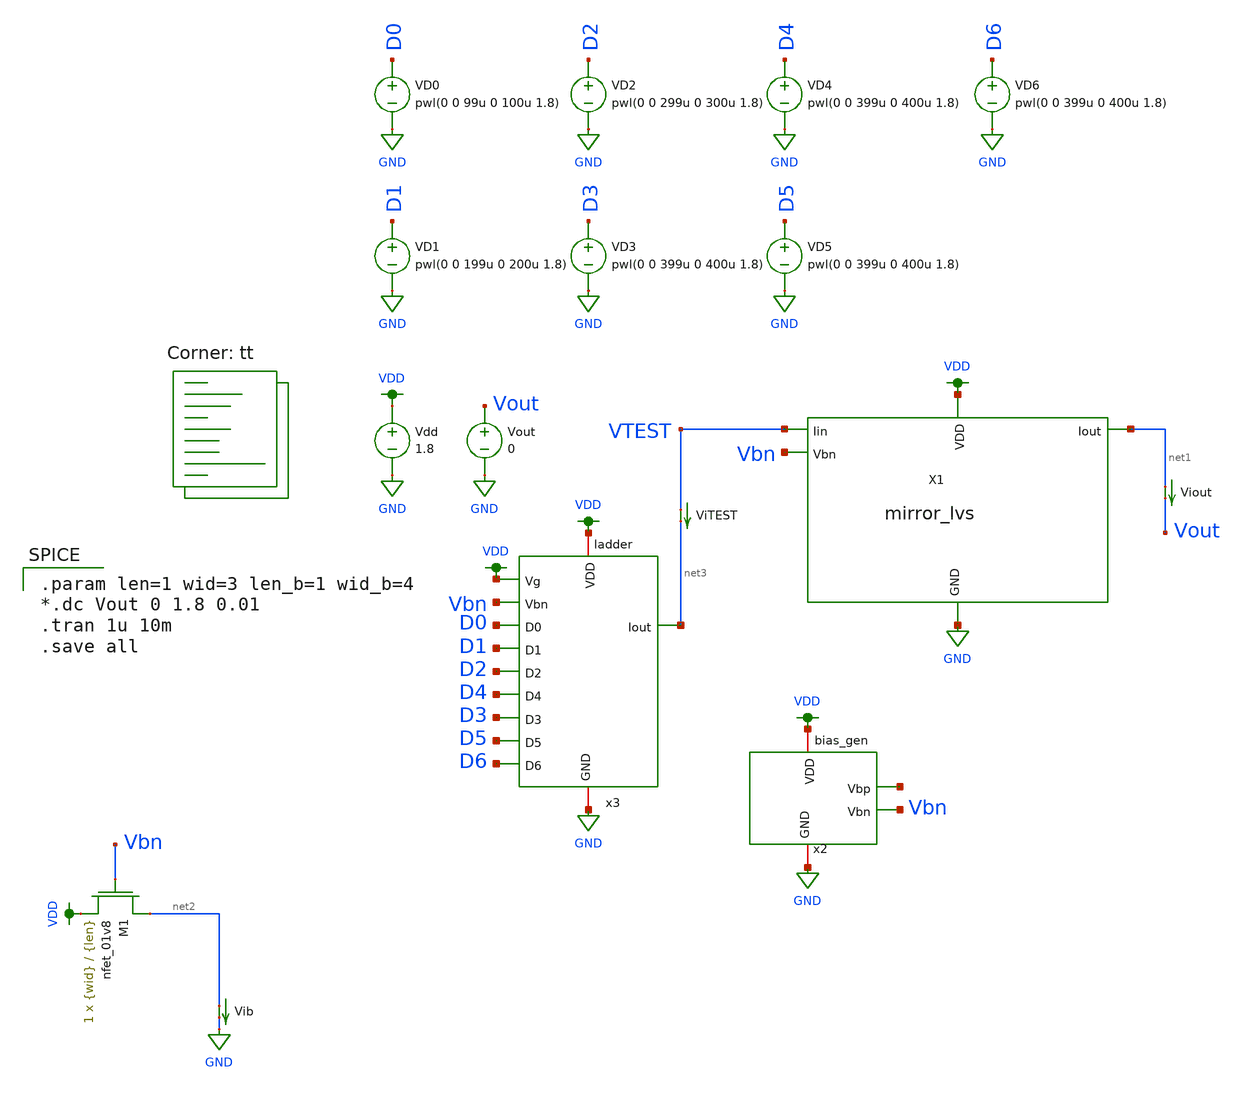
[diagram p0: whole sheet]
** sch_path: mp3/dac_tb.sch
**.subckt dac_tb
X1 net1 VTEST GND Vbn VDD mirror_lvs
Vdd VDD GND 1.8
Vout Vout GND 0
ViTEST VTEST net3 0
.save i(vitest)
x2 VDD net4 Vbn GND bias_gen
x3 net3 VDD VDD D1 D0 D2 D4 D3 D5 D6 Vbn GND ladder
VD0 D0 GND pwl(0 0 99u 0 100u 1.8)
VD1 D1 GND pwl(0 0 199u 0 200u 1.8)
VD2 D2 GND pwl(0 0 299u 0 300u 1.8)
VD3 D3 GND pwl(0 0 399u 0 400u 1.8)
VD4 D4 GND pwl(0 0 399u 0 400u 1.8)
VD5 D5 GND pwl(0 0 399u 0 400u 1.8)
VD6 D6 GND pwl(0 0 399u 0 400u 1.8)
XM1 net2 Vbn VDD GND sky130_fd_pr__nfet_01v8 L={len} W={wid} nf=1 ad='int((nf+1)/2) * W/nf * 0.29' as='int((nf+2)/2) * W/nf * 0.29'
+ pd='2*int((nf+1)/2) * (W/nf + 0.29)' ps='2*int((nf+2)/2) * (W/nf + 0.29)' nrd='0.29 / W' nrs='0.29 / W'
+ sa=0 sb=0 sd=0 mult=1 m=1
Vib net2 GND 0
.save i(vib)
Viout net1 Vout 0
.save i(viout)
**** begin user architecture code
.lib $::SKYWATER_MODELS/sky130.lib.spice tt

.param len=1 wid=3 len_b=1 wid_b=4
*.dc Vout 0 1.8 0.01
.tran 1u 10m
.save all


**** end user architecture code
**.ends

* expanding   symbol:  mirror_lvs.sym # of pins=5
** sym_path: mp3/mirror_lvs.sym
** sch_path: mp3/mirror_lvs.sch
.subckt mirror_lvs Iout Iin GND Vbn VDD
*.ipin Vbn
*.ipin Iin
*.iopin GND
*.iopin GND
*.iopin GND
*.iopin GND
*.iopin VDD
*.iopin VDD
*.iopin VDD
*.opin Iout
XM1 net4 net4 net5 VDD sky130_fd_pr__pfet_01v8 L={len} W={wid} nf=1 ad='int((nf+1)/2) * W/nf * 0.29'
+ as='int((nf+2)/2) * W/nf * 0.29' pd='2*int((nf+1)/2) * (W/nf + 0.29)' ps='2*int((nf+2)/2) * (W/nf + 0.29)'
+ nrd='0.29 / W' nrs='0.29 / W' sa=0 sb=0 sd=0 mult=1 m=1
XM2 net4 net1 net3 GND sky130_fd_pr__nfet_01v8 L={len} W={wid} nf=1 ad='int((nf+1)/2) * W/nf * 0.29'
+ as='int((nf+2)/2) * W/nf * 0.29' pd='2*int((nf+1)/2) * (W/nf + 0.29)' ps='2*int((nf+2)/2) * (W/nf + 0.29)'
+ nrd='0.29 / W' nrs='0.29 / W' sa=0 sb=0 sd=0 mult=1 m=1
XM3 net3 net1 net2 GND sky130_fd_pr__nfet_01v8 L={len} W={wid} nf=1 ad='int((nf+1)/2) * W/nf * 0.29'
+ as='int((nf+2)/2) * W/nf * 0.29' pd='2*int((nf+1)/2) * (W/nf + 0.29)' ps='2*int((nf+2)/2) * (W/nf + 0.29)'
+ nrd='0.29 / W' nrs='0.29 / W' sa=0 sb=0 sd=0 mult=1 m=1
XM4 net2 net1 GND GND sky130_fd_pr__nfet_01v8 L={len} W={wid} nf=1 ad='int((nf+1)/2) * W/nf * 0.29' as='int((nf+2)/2) * W/nf * 0.29'
+ pd='2*int((nf+1)/2) * (W/nf + 0.29)' ps='2*int((nf+2)/2) * (W/nf + 0.29)' nrd='0.29 / W' nrs='0.29 / W'
+ sa=0 sb=0 sd=0 mult=1 m=1
XM5 GND net1 net7 GND sky130_fd_pr__nfet_01v8 L={len} W={wid} nf=1 ad='int((nf+1)/2) * W/nf * 0.29' as='int((nf+2)/2) * W/nf * 0.29'
+ pd='2*int((nf+1)/2) * (W/nf + 0.29)' ps='2*int((nf+2)/2) * (W/nf + 0.29)' nrd='0.29 / W' nrs='0.29 / W'
+ sa=0 sb=0 sd=0 mult=1 m=1
XM6 net8 net1 GND GND sky130_fd_pr__nfet_01v8 L={len} W={wid} nf=1 ad='int((nf+1)/2) * W/nf * 0.29' as='int((nf+2)/2) * W/nf * 0.29'
+ pd='2*int((nf+1)/2) * (W/nf + 0.29)' ps='2*int((nf+2)/2) * (W/nf + 0.29)' nrd='0.29 / W' nrs='0.29 / W'
+ sa=0 sb=0 sd=0 mult=1 m=1
XM7 GND net1 net9 GND sky130_fd_pr__nfet_01v8 L={len} W={wid} nf=1 ad='int((nf+1)/2) * W/nf * 0.29' as='int((nf+2)/2) * W/nf * 0.29'
+ pd='2*int((nf+1)/2) * (W/nf + 0.29)' ps='2*int((nf+2)/2) * (W/nf + 0.29)' nrd='0.29 / W' nrs='0.29 / W'
+ sa=0 sb=0 sd=0 mult=1 m=1
XM8 net5 net4 VDD VDD sky130_fd_pr__pfet_01v8 L={len} W={wid} nf=1 ad='int((nf+1)/2) * W/nf * 0.29' as='int((nf+2)/2) * W/nf * 0.29'
+ pd='2*int((nf+1)/2) * (W/nf + 0.29)' ps='2*int((nf+2)/2) * (W/nf + 0.29)' nrd='0.29 / W' nrs='0.29 / W'
+ sa=0 sb=0 sd=0 mult=1 m=1
XM9 net5 net4 net4 VDD sky130_fd_pr__pfet_01v8 L={len} W={wid} nf=1 ad='int((nf+1)/2) * W/nf * 0.29'
+ as='int((nf+2)/2) * W/nf * 0.29' pd='2*int((nf+1)/2) * (W/nf + 0.29)' ps='2*int((nf+2)/2) * (W/nf + 0.29)'
+ nrd='0.29 / W' nrs='0.29 / W' sa=0 sb=0 sd=0 mult=1 m=1
XM10 net7 net7 net5 VDD sky130_fd_pr__pfet_01v8 L={len} W={wid} nf=1 ad='int((nf+1)/2) * W/nf * 0.29'
+ as='int((nf+2)/2) * W/nf * 0.29' pd='2*int((nf+1)/2) * (W/nf + 0.29)' ps='2*int((nf+2)/2) * (W/nf + 0.29)'
+ nrd='0.29 / W' nrs='0.29 / W' sa=0 sb=0 sd=0 mult=1 m=1
XM11 Iin net9 VDD VDD sky130_fd_pr__pfet_01v8 L={len} W={wid} nf=1 ad='int((nf+1)/2) * W/nf * 0.29' as='int((nf+2)/2) * W/nf * 0.29'
+ pd='2*int((nf+1)/2) * (W/nf + 0.29)' ps='2*int((nf+2)/2) * (W/nf + 0.29)' nrd='0.29 / W' nrs='0.29 / W'
+ sa=0 sb=0 sd=0 mult=1 m=1
XM12 Iin net7 net8 VDD sky130_fd_pr__pfet_01v8 L={len} W={wid} nf=1 ad='int((nf+1)/2) * W/nf * 0.29'
+ as='int((nf+2)/2) * W/nf * 0.29' pd='2*int((nf+1)/2) * (W/nf + 0.29)' ps='2*int((nf+2)/2) * (W/nf + 0.29)'
+ nrd='0.29 / W' nrs='0.29 / W' sa=0 sb=0 sd=0 mult=1 m=1
XM13 VDD net9 net6 VDD sky130_fd_pr__pfet_01v8 L={len} W={wid} nf=1 ad='int((nf+1)/2) * W/nf * 0.29'
+ as='int((nf+2)/2) * W/nf * 0.29' pd='2*int((nf+1)/2) * (W/nf + 0.29)' ps='2*int((nf+2)/2) * (W/nf + 0.29)'
+ nrd='0.29 / W' nrs='0.29 / W' sa=0 sb=0 sd=0 mult=1 m=1
XM14 net9 net7 net6 VDD sky130_fd_pr__pfet_01v8 L={len} W={wid} nf=1 ad='int((nf+1)/2) * W/nf * 0.29'
+ as='int((nf+2)/2) * W/nf * 0.29' pd='2*int((nf+1)/2) * (W/nf + 0.29)' ps='2*int((nf+2)/2) * (W/nf + 0.29)'
+ nrd='0.29 / W' nrs='0.29 / W' sa=0 sb=0 sd=0 mult=1 m=1
XM15 net6 net8 Iout VDD sky130_fd_pr__pfet_01v8 L={len} W={wid} nf=1 ad='int((nf+1)/2) * W/nf * 0.29'
+ as='int((nf+2)/2) * W/nf * 0.29' pd='2*int((nf+1)/2) * (W/nf + 0.29)' ps='2*int((nf+2)/2) * (W/nf + 0.29)'
+ nrd='0.29 / W' nrs='0.29 / W' sa=0 sb=0 sd=0 mult=1 m=1
XM16 net12 net12 net13 VDD sky130_fd_pr__pfet_01v8 L={len} W={wid} nf=1 ad='int((nf+1)/2) * W/nf * 0.29'
+ as='int((nf+2)/2) * W/nf * 0.29' pd='2*int((nf+1)/2) * (W/nf + 0.29)' ps='2*int((nf+2)/2) * (W/nf + 0.29)'
+ nrd='0.29 / W' nrs='0.29 / W' sa=0 sb=0 sd=0 mult=1 m=1
XM17 net12 Vbn net11 GND sky130_fd_pr__nfet_01v8 L={len} W={wid} nf=1 ad='int((nf+1)/2) * W/nf * 0.29'
+ as='int((nf+2)/2) * W/nf * 0.29' pd='2*int((nf+1)/2) * (W/nf + 0.29)' ps='2*int((nf+2)/2) * (W/nf + 0.29)'
+ nrd='0.29 / W' nrs='0.29 / W' sa=0 sb=0 sd=0 mult=1 m=1
XM18 net11 Vbn net10 GND sky130_fd_pr__nfet_01v8 L={len} W={wid} nf=1 ad='int((nf+1)/2) * W/nf * 0.29'
+ as='int((nf+2)/2) * W/nf * 0.29' pd='2*int((nf+1)/2) * (W/nf + 0.29)' ps='2*int((nf+2)/2) * (W/nf + 0.29)'
+ nrd='0.29 / W' nrs='0.29 / W' sa=0 sb=0 sd=0 mult=1 m=1
XM19 net10 Vbn GND GND sky130_fd_pr__nfet_01v8 L={len} W={wid} nf=1 ad='int((nf+1)/2) * W/nf * 0.29'
+ as='int((nf+2)/2) * W/nf * 0.29' pd='2*int((nf+1)/2) * (W/nf + 0.29)' ps='2*int((nf+2)/2) * (W/nf + 0.29)'
+ nrd='0.29 / W' nrs='0.29 / W' sa=0 sb=0 sd=0 mult=1 m=1
XM20 GND Vbn net15 GND sky130_fd_pr__nfet_01v8 L={len} W={wid} nf=1 ad='int((nf+1)/2) * W/nf * 0.29'
+ as='int((nf+2)/2) * W/nf * 0.29' pd='2*int((nf+1)/2) * (W/nf + 0.29)' ps='2*int((nf+2)/2) * (W/nf + 0.29)'
+ nrd='0.29 / W' nrs='0.29 / W' sa=0 sb=0 sd=0 mult=1 m=1
XM21 net16 Vbn GND GND sky130_fd_pr__nfet_01v8 L={len} W={wid} nf=1 ad='int((nf+1)/2) * W/nf * 0.29'
+ as='int((nf+2)/2) * W/nf * 0.29' pd='2*int((nf+1)/2) * (W/nf + 0.29)' ps='2*int((nf+2)/2) * (W/nf + 0.29)'
+ nrd='0.29 / W' nrs='0.29 / W' sa=0 sb=0 sd=0 mult=1 m=1
XM22 GND Vbn net17 GND sky130_fd_pr__nfet_01v8 L={len} W={wid} nf=1 ad='int((nf+1)/2) * W/nf * 0.29'
+ as='int((nf+2)/2) * W/nf * 0.29' pd='2*int((nf+1)/2) * (W/nf + 0.29)' ps='2*int((nf+2)/2) * (W/nf + 0.29)'
+ nrd='0.29 / W' nrs='0.29 / W' sa=0 sb=0 sd=0 mult=1 m=1
XM23 net13 net12 VDD VDD sky130_fd_pr__pfet_01v8 L={len} W={wid} nf=1 ad='int((nf+1)/2) * W/nf * 0.29'
+ as='int((nf+2)/2) * W/nf * 0.29' pd='2*int((nf+1)/2) * (W/nf + 0.29)' ps='2*int((nf+2)/2) * (W/nf + 0.29)'
+ nrd='0.29 / W' nrs='0.29 / W' sa=0 sb=0 sd=0 mult=1 m=1
XM24 net13 net12 net12 VDD sky130_fd_pr__pfet_01v8 L={len} W={wid} nf=1 ad='int((nf+1)/2) * W/nf * 0.29'
+ as='int((nf+2)/2) * W/nf * 0.29' pd='2*int((nf+1)/2) * (W/nf + 0.29)' ps='2*int((nf+2)/2) * (W/nf + 0.29)'
+ nrd='0.29 / W' nrs='0.29 / W' sa=0 sb=0 sd=0 mult=1 m=1
XM25 net15 net15 net13 VDD sky130_fd_pr__pfet_01v8 L={len} W={wid} nf=1 ad='int((nf+1)/2) * W/nf * 0.29'
+ as='int((nf+2)/2) * W/nf * 0.29' pd='2*int((nf+1)/2) * (W/nf + 0.29)' ps='2*int((nf+2)/2) * (W/nf + 0.29)'
+ nrd='0.29 / W' nrs='0.29 / W' sa=0 sb=0 sd=0 mult=1 m=1
XM26 Iin net17 VDD VDD sky130_fd_pr__pfet_01v8 L={len} W={wid} nf=1 ad='int((nf+1)/2) * W/nf * 0.29'
+ as='int((nf+2)/2) * W/nf * 0.29' pd='2*int((nf+1)/2) * (W/nf + 0.29)' ps='2*int((nf+2)/2) * (W/nf + 0.29)'
+ nrd='0.29 / W' nrs='0.29 / W' sa=0 sb=0 sd=0 mult=1 m=1
XM27 Iin net15 net16 VDD sky130_fd_pr__pfet_01v8 L={len} W={wid} nf=1 ad='int((nf+1)/2) * W/nf * 0.29'
+ as='int((nf+2)/2) * W/nf * 0.29' pd='2*int((nf+1)/2) * (W/nf + 0.29)' ps='2*int((nf+2)/2) * (W/nf + 0.29)'
+ nrd='0.29 / W' nrs='0.29 / W' sa=0 sb=0 sd=0 mult=1 m=1
XM28 VDD net17 net14 VDD sky130_fd_pr__pfet_01v8 L={len} W={wid} nf=1 ad='int((nf+1)/2) * W/nf * 0.29'
+ as='int((nf+2)/2) * W/nf * 0.29' pd='2*int((nf+1)/2) * (W/nf + 0.29)' ps='2*int((nf+2)/2) * (W/nf + 0.29)'
+ nrd='0.29 / W' nrs='0.29 / W' sa=0 sb=0 sd=0 mult=1 m=1
XM29 net17 net15 net14 VDD sky130_fd_pr__pfet_01v8 L={len} W={wid} nf=1 ad='int((nf+1)/2) * W/nf * 0.29'
+ as='int((nf+2)/2) * W/nf * 0.29' pd='2*int((nf+1)/2) * (W/nf + 0.29)' ps='2*int((nf+2)/2) * (W/nf + 0.29)'
+ nrd='0.29 / W' nrs='0.29 / W' sa=0 sb=0 sd=0 mult=1 m=1
XM30 net14 net16 Iout VDD sky130_fd_pr__pfet_01v8 L={len} W={wid} nf=1 ad='int((nf+1)/2) * W/nf * 0.29'
+ as='int((nf+2)/2) * W/nf * 0.29' pd='2*int((nf+1)/2) * (W/nf + 0.29)' ps='2*int((nf+2)/2) * (W/nf + 0.29)'
+ nrd='0.29 / W' nrs='0.29 / W' sa=0 sb=0 sd=0 mult=1 m=1
.ends


* expanding   symbol:  bias_gen.sym # of pins=4
** sym_path: mp3/bias_gen.sym
** sch_path: mp3/bias_gen.sch
.subckt bias_gen VDD Vbp Vbn GND
*.iopin GND
*.iopin VDD
*.opin Vbn
*.opin Vbp
XM1 net3 net1 net1 GND sky130_fd_pr__nfet_01v8 L={len} W={wid} nf=1 ad='int((nf+1)/2) * W/nf * 0.29'
+ as='int((nf+2)/2) * W/nf * 0.29' pd='2*int((nf+1)/2) * (W/nf + 0.29)' ps='2*int((nf+2)/2) * (W/nf + 0.29)'
+ nrd='0.29 / W' nrs='0.29 / W' sa=0 sb=0 sd=0 mult=8 m=8
XM4 Vbn Vbn GND GND sky130_fd_pr__nfet_01v8 L={len} W={wid} nf=1 ad='int((nf+1)/2) * W/nf * 0.29' as='int((nf+2)/2) * W/nf * 0.29'
+ pd='2*int((nf+1)/2) * (W/nf + 0.29)' ps='2*int((nf+2)/2) * (W/nf + 0.29)' nrd='0.29 / W' nrs='0.29 / W'
+ sa=0 sb=0 sd=0 mult=1 m=1
XM5 GND Vbp GND GND sky130_fd_pr__nfet_01v8 L=10 W=10 nf=1 ad='int((nf+1)/2) * W/nf * 0.29' as='int((nf+2)/2) * W/nf * 0.29'
+ pd='2*int((nf+1)/2) * (W/nf + 0.29)' ps='2*int((nf+2)/2) * (W/nf + 0.29)' nrd='0.29 / W' nrs='0.29 / W'
+ sa=0 sb=0 sd=0 mult=1 m=1
XM6 VDD Vbp net1 VDD sky130_fd_pr__pfet_01v8 L={len} W={wid} nf=1 ad='int((nf+1)/2) * W/nf * 0.29' as='int((nf+2)/2) * W/nf * 0.29'
+ pd='2*int((nf+1)/2) * (W/nf + 0.29)' ps='2*int((nf+2)/2) * (W/nf + 0.29)' nrd='0.29 / W' nrs='0.29 / W'
+ sa=0 sb=0 sd=0 mult=1 m=1
R1 net3 GND 100k m=1
XM2 GND Vbn Vbp GND sky130_fd_pr__nfet_01v8 L={len} W={wid} nf=1 ad='int((nf+1)/2) * W/nf * 0.29' as='int((nf+2)/2) * W/nf * 0.29'
+ pd='2*int((nf+1)/2) * (W/nf + 0.29)' ps='2*int((nf+2)/2) * (W/nf + 0.29)' nrd='0.29 / W' nrs='0.29 / W'
+ sa=0 sb=0 sd=0 mult=1 m=1
XM3 net2 net1 GND GND sky130_fd_pr__nfet_01v8 L={len} W={wid} nf=1 ad='int((nf+1)/2) * W/nf * 0.29' as='int((nf+2)/2) * W/nf * 0.29'
+ pd='2*int((nf+1)/2) * (W/nf + 0.29)' ps='2*int((nf+2)/2) * (W/nf + 0.29)' nrd='0.29 / W' nrs='0.29 / W'
+ sa=0 sb=0 sd=0 mult=1 m=1
XM7 VDD net2 net2 VDD sky130_fd_pr__pfet_01v8 L={len} W={wid} nf=1 ad='int((nf+1)/2) * W/nf * 0.29' as='int((nf+2)/2) * W/nf * 0.29'
+ pd='2*int((nf+1)/2) * (W/nf + 0.29)' ps='2*int((nf+2)/2) * (W/nf + 0.29)' nrd='0.29 / W' nrs='0.29 / W'
+ sa=0 sb=0 sd=0 mult=1 m=1
XM8 Vbp net2 VDD VDD sky130_fd_pr__pfet_01v8 L={len} W={wid} nf=1 ad='int((nf+1)/2) * W/nf * 0.29' as='int((nf+2)/2) * W/nf * 0.29'
+ pd='2*int((nf+1)/2) * (W/nf + 0.29)' ps='2*int((nf+2)/2) * (W/nf + 0.29)' nrd='0.29 / W' nrs='0.29 / W'
+ sa=0 sb=0 sd=0 mult=1 m=1
XM9 net4 Vbp VDD VDD sky130_fd_pr__pfet_01v8 L={len} W={wid} nf=1 ad='int((nf+1)/2) * W/nf * 0.29' as='int((nf+2)/2) * W/nf * 0.29'
+ pd='2*int((nf+1)/2) * (W/nf + 0.29)' ps='2*int((nf+2)/2) * (W/nf + 0.29)' nrd='0.29 / W' nrs='0.29 / W'
+ sa=0 sb=0 sd=0 mult=1 m=1
Vib net4 Vbn 0
.save i(vib)
.ends


* expanding   symbol:  ladder.sym # of pins=12
** sym_path: mp3/ladder.sym
** sch_path: mp3/ladder.sch
.subckt ladder Iout VDD Vg D1 D0 D2 D4 D3 D5 D6 Vbn GND
*.ipin Vbn
*.iopin VDD
*.opin Iout
*.iopin GND
*.ipin D0
*.ipin D1
*.ipin D2
*.ipin D3
*.ipin D4
*.ipin D5
*.ipin D6
*.ipin Vg
XM1 net5 Vg VDD GND sky130_fd_pr__nfet_01v8 L={len} W={wid} nf=1 ad='int((nf+1)/2) * W/nf * 0.29' as='int((nf+2)/2) * W/nf * 0.29'
+ pd='2*int((nf+1)/2) * (W/nf + 0.29)' ps='2*int((nf+2)/2) * (W/nf + 0.29)' nrd='0.29 / W' nrs='0.29 / W'
+ sa=0 sb=0 sd=0 mult=1 m=1
XM4 net5 Vg net7 GND sky130_fd_pr__nfet_01v8 L={len} W={wid} nf=1 ad='int((nf+1)/2) * W/nf * 0.29' as='int((nf+2)/2) * W/nf * 0.29'
+ pd='2*int((nf+1)/2) * (W/nf + 0.29)' ps='2*int((nf+2)/2) * (W/nf + 0.29)' nrd='0.29 / W' nrs='0.29 / W'
+ sa=0 sb=0 sd=0 mult=1 m=1
XM12 net28 Vbn net15 GND sky130_fd_pr__nfet_01v8 L={len_b} W={wid_b} nf=1 ad='int((nf+1)/2) * W/nf * 0.29'
+ as='int((nf+2)/2) * W/nf * 0.29' pd='2*int((nf+1)/2) * (W/nf + 0.29)' ps='2*int((nf+2)/2) * (W/nf + 0.29)'
+ nrd='0.29 / W' nrs='0.29 / W' sa=0 sb=0 sd=0 mult=1 m=1
XM2 VDD Vg net5 GND sky130_fd_pr__nfet_01v8 L={len} W={wid} nf=1 ad='int((nf+1)/2) * W/nf * 0.29' as='int((nf+2)/2) * W/nf * 0.29'
+ pd='2*int((nf+1)/2) * (W/nf + 0.29)' ps='2*int((nf+2)/2) * (W/nf + 0.29)' nrd='0.29 / W' nrs='0.29 / W'
+ sa=0 sb=0 sd=0 mult=1 m=1
XM18 net7 Vg VDD GND sky130_fd_pr__nfet_01v8 L={len} W={wid} nf=1 ad='int((nf+1)/2) * W/nf * 0.29' as='int((nf+2)/2) * W/nf * 0.29'
+ pd='2*int((nf+1)/2) * (W/nf + 0.29)' ps='2*int((nf+2)/2) * (W/nf + 0.29)' nrd='0.29 / W' nrs='0.29 / W'
+ sa=0 sb=0 sd=0 mult=1 m=1
XM19 net9 Vg VDD GND sky130_fd_pr__nfet_01v8 L={len} W={wid} nf=1 ad='int((nf+1)/2) * W/nf * 0.29' as='int((nf+2)/2) * W/nf * 0.29'
+ pd='2*int((nf+1)/2) * (W/nf + 0.29)' ps='2*int((nf+2)/2) * (W/nf + 0.29)' nrd='0.29 / W' nrs='0.29 / W'
+ sa=0 sb=0 sd=0 mult=1 m=1
XM20 net13 Vg VDD GND sky130_fd_pr__nfet_01v8 L={len} W={wid} nf=1 ad='int((nf+1)/2) * W/nf * 0.29' as='int((nf+2)/2) * W/nf * 0.29'
+ pd='2*int((nf+1)/2) * (W/nf + 0.29)' ps='2*int((nf+2)/2) * (W/nf + 0.29)' nrd='0.29 / W' nrs='0.29 / W'
+ sa=0 sb=0 sd=0 mult=1 m=1
XM21 net14 Vg VDD GND sky130_fd_pr__nfet_01v8 L={len} W={wid} nf=1 ad='int((nf+1)/2) * W/nf * 0.29' as='int((nf+2)/2) * W/nf * 0.29'
+ pd='2*int((nf+1)/2) * (W/nf + 0.29)' ps='2*int((nf+2)/2) * (W/nf + 0.29)' nrd='0.29 / W' nrs='0.29 / W'
+ sa=0 sb=0 sd=0 mult=1 m=1
XM22 net8 Vg VDD GND sky130_fd_pr__nfet_01v8 L={len} W={wid} nf=1 ad='int((nf+1)/2) * W/nf * 0.29' as='int((nf+2)/2) * W/nf * 0.29'
+ pd='2*int((nf+1)/2) * (W/nf + 0.29)' ps='2*int((nf+2)/2) * (W/nf + 0.29)' nrd='0.29 / W' nrs='0.29 / W'
+ sa=0 sb=0 sd=0 mult=1 m=1
XM23 net6 Vg Iout GND sky130_fd_pr__nfet_01v8 L={len} W={wid} nf=1 ad='int((nf+1)/2) * W/nf * 0.29' as='int((nf+2)/2) * W/nf * 0.29'
+ pd='2*int((nf+1)/2) * (W/nf + 0.29)' ps='2*int((nf+2)/2) * (W/nf + 0.29)' nrd='0.29 / W' nrs='0.29 / W'
+ sa=0 sb=0 sd=0 mult=1 m=1
XM24 Iout Vg net6 GND sky130_fd_pr__nfet_01v8 L={len} W={wid} nf=1 ad='int((nf+1)/2) * W/nf * 0.29' as='int((nf+2)/2) * W/nf * 0.29'
+ pd='2*int((nf+1)/2) * (W/nf + 0.29)' ps='2*int((nf+2)/2) * (W/nf + 0.29)' nrd='0.29 / W' nrs='0.29 / W'
+ sa=0 sb=0 sd=0 mult=1 m=1
XM3 net7 Vg net5 GND sky130_fd_pr__nfet_01v8 L={len} W={wid} nf=1 ad='int((nf+1)/2) * W/nf * 0.29' as='int((nf+2)/2) * W/nf * 0.29'
+ pd='2*int((nf+1)/2) * (W/nf + 0.29)' ps='2*int((nf+2)/2) * (W/nf + 0.29)' nrd='0.29 / W' nrs='0.29 / W'
+ sa=0 sb=0 sd=0 mult=1 m=1
XM5 net7 Vg net9 GND sky130_fd_pr__nfet_01v8 L={len} W={wid} nf=1 ad='int((nf+1)/2) * W/nf * 0.29' as='int((nf+2)/2) * W/nf * 0.29'
+ pd='2*int((nf+1)/2) * (W/nf + 0.29)' ps='2*int((nf+2)/2) * (W/nf + 0.29)' nrd='0.29 / W' nrs='0.29 / W'
+ sa=0 sb=0 sd=0 mult=1 m=1
XM6 net9 Vg net7 GND sky130_fd_pr__nfet_01v8 L={len} W={wid} nf=1 ad='int((nf+1)/2) * W/nf * 0.29' as='int((nf+2)/2) * W/nf * 0.29'
+ pd='2*int((nf+1)/2) * (W/nf + 0.29)' ps='2*int((nf+2)/2) * (W/nf + 0.29)' nrd='0.29 / W' nrs='0.29 / W'
+ sa=0 sb=0 sd=0 mult=1 m=1
XM7 net9 Vg net13 GND sky130_fd_pr__nfet_01v8 L={len} W={wid} nf=1 ad='int((nf+1)/2) * W/nf * 0.29' as='int((nf+2)/2) * W/nf * 0.29'
+ pd='2*int((nf+1)/2) * (W/nf + 0.29)' ps='2*int((nf+2)/2) * (W/nf + 0.29)' nrd='0.29 / W' nrs='0.29 / W'
+ sa=0 sb=0 sd=0 mult=1 m=1
XM17 net13 Vg net9 GND sky130_fd_pr__nfet_01v8 L={len} W={wid} nf=1 ad='int((nf+1)/2) * W/nf * 0.29'
+ as='int((nf+2)/2) * W/nf * 0.29' pd='2*int((nf+1)/2) * (W/nf + 0.29)' ps='2*int((nf+2)/2) * (W/nf + 0.29)'
+ nrd='0.29 / W' nrs='0.29 / W' sa=0 sb=0 sd=0 mult=1 m=1
XM31 net13 Vg net14 GND sky130_fd_pr__nfet_01v8 L={len} W={wid} nf=1 ad='int((nf+1)/2) * W/nf * 0.29'
+ as='int((nf+2)/2) * W/nf * 0.29' pd='2*int((nf+1)/2) * (W/nf + 0.29)' ps='2*int((nf+2)/2) * (W/nf + 0.29)'
+ nrd='0.29 / W' nrs='0.29 / W' sa=0 sb=0 sd=0 mult=1 m=1
XM32 net14 Vg net13 GND sky130_fd_pr__nfet_01v8 L={len} W={wid} nf=1 ad='int((nf+1)/2) * W/nf * 0.29'
+ as='int((nf+2)/2) * W/nf * 0.29' pd='2*int((nf+1)/2) * (W/nf + 0.29)' ps='2*int((nf+2)/2) * (W/nf + 0.29)'
+ nrd='0.29 / W' nrs='0.29 / W' sa=0 sb=0 sd=0 mult=1 m=1
XM33 net14 Vg net8 GND sky130_fd_pr__nfet_01v8 L={len} W={wid} nf=1 ad='int((nf+1)/2) * W/nf * 0.29'
+ as='int((nf+2)/2) * W/nf * 0.29' pd='2*int((nf+1)/2) * (W/nf + 0.29)' ps='2*int((nf+2)/2) * (W/nf + 0.29)'
+ nrd='0.29 / W' nrs='0.29 / W' sa=0 sb=0 sd=0 mult=1 m=1
XM34 net8 Vg net14 GND sky130_fd_pr__nfet_01v8 L={len} W={wid} nf=1 ad='int((nf+1)/2) * W/nf * 0.29'
+ as='int((nf+2)/2) * W/nf * 0.29' pd='2*int((nf+1)/2) * (W/nf + 0.29)' ps='2*int((nf+2)/2) * (W/nf + 0.29)'
+ nrd='0.29 / W' nrs='0.29 / W' sa=0 sb=0 sd=0 mult=1 m=1
XM35 net8 Vg net6 GND sky130_fd_pr__nfet_01v8 L={len} W={wid} nf=1 ad='int((nf+1)/2) * W/nf * 0.29' as='int((nf+2)/2) * W/nf * 0.29'
+ pd='2*int((nf+1)/2) * (W/nf + 0.29)' ps='2*int((nf+2)/2) * (W/nf + 0.29)' nrd='0.29 / W' nrs='0.29 / W'
+ sa=0 sb=0 sd=0 mult=1 m=1
XM36 net6 Vg net8 GND sky130_fd_pr__nfet_01v8 L={len} W={wid} nf=1 ad='int((nf+1)/2) * W/nf * 0.29' as='int((nf+2)/2) * W/nf * 0.29'
+ pd='2*int((nf+1)/2) * (W/nf + 0.29)' ps='2*int((nf+2)/2) * (W/nf + 0.29)' nrd='0.29 / W' nrs='0.29 / W'
+ sa=0 sb=0 sd=0 mult=1 m=1
Vib0 net15 GND 0
.save i(vib0)
**** begin user architecture code

.param len=4 wid=2 len_b=3.6 wid_b=2 len_p=4 wid_p=1

**** end user architecture code
Vib1 net16 GND 0
.save i(vib1)
Vib2 net17 GND 0
.save i(vib2)
Vib3 net18 GND 0
.save i(vib3)
Vib4 net19 GND 0
.save i(vib4)
Vib5 net20 GND 0
.save i(vib5)
Vib6 net21 GND 0
.save i(vib6)
XM16 net1 D0 net28 GND sky130_fd_pr__nfet_01v8 L={len_p} W={wid_p} nf=1 ad='int((nf+1)/2) * W/nf * 0.29'
+ as='int((nf+2)/2) * W/nf * 0.29' pd='2*int((nf+1)/2) * (W/nf + 0.29)' ps='2*int((nf+2)/2) * (W/nf + 0.29)'
+ nrd='0.29 / W' nrs='0.29 / W' sa=0 sb=0 sd=0 mult=1 m=1
XM8 net5 D0 net1 GND sky130_fd_pr__nfet_01v8 L={len_p} W={wid_p} nf=1 ad='int((nf+1)/2) * W/nf * 0.29'
+ as='int((nf+2)/2) * W/nf * 0.29' pd='2*int((nf+1)/2) * (W/nf + 0.29)' ps='2*int((nf+2)/2) * (W/nf + 0.29)'
+ nrd='0.29 / W' nrs='0.29 / W' sa=0 sb=0 sd=0 mult=1 m=1
XM9 net7 D1 net2 GND sky130_fd_pr__nfet_01v8 L={len_p} W={wid_p} nf=1 ad='int((nf+1)/2) * W/nf * 0.29'
+ as='int((nf+2)/2) * W/nf * 0.29' pd='2*int((nf+1)/2) * (W/nf + 0.29)' ps='2*int((nf+2)/2) * (W/nf + 0.29)'
+ nrd='0.29 / W' nrs='0.29 / W' sa=0 sb=0 sd=0 mult=1 m=1
XM10 net2 D1 net27 GND sky130_fd_pr__nfet_01v8 L={len_p} W={wid_p} nf=1 ad='int((nf+1)/2) * W/nf * 0.29'
+ as='int((nf+2)/2) * W/nf * 0.29' pd='2*int((nf+1)/2) * (W/nf + 0.29)' ps='2*int((nf+2)/2) * (W/nf + 0.29)'
+ nrd='0.29 / W' nrs='0.29 / W' sa=0 sb=0 sd=0 mult=1 m=1
XM11 net3 D2 net26 GND sky130_fd_pr__nfet_01v8 L={len_p} W={wid_p} nf=1 ad='int((nf+1)/2) * W/nf * 0.29'
+ as='int((nf+2)/2) * W/nf * 0.29' pd='2*int((nf+1)/2) * (W/nf + 0.29)' ps='2*int((nf+2)/2) * (W/nf + 0.29)'
+ nrd='0.29 / W' nrs='0.29 / W' sa=0 sb=0 sd=0 mult=1 m=1
XM13 net9 D2 net3 GND sky130_fd_pr__nfet_01v8 L={len_p} W={wid_p} nf=1 ad='int((nf+1)/2) * W/nf * 0.29'
+ as='int((nf+2)/2) * W/nf * 0.29' pd='2*int((nf+1)/2) * (W/nf + 0.29)' ps='2*int((nf+2)/2) * (W/nf + 0.29)'
+ nrd='0.29 / W' nrs='0.29 / W' sa=0 sb=0 sd=0 mult=1 m=1
XM14 net13 D3 net4 GND sky130_fd_pr__nfet_01v8 L={len_p} W={wid_p} nf=1 ad='int((nf+1)/2) * W/nf * 0.29'
+ as='int((nf+2)/2) * W/nf * 0.29' pd='2*int((nf+1)/2) * (W/nf + 0.29)' ps='2*int((nf+2)/2) * (W/nf + 0.29)'
+ nrd='0.29 / W' nrs='0.29 / W' sa=0 sb=0 sd=0 mult=1 m=1
XM15 net4 D3 net25 GND sky130_fd_pr__nfet_01v8 L={len_p} W={wid_p} nf=1 ad='int((nf+1)/2) * W/nf * 0.29'
+ as='int((nf+2)/2) * W/nf * 0.29' pd='2*int((nf+1)/2) * (W/nf + 0.29)' ps='2*int((nf+2)/2) * (W/nf + 0.29)'
+ nrd='0.29 / W' nrs='0.29 / W' sa=0 sb=0 sd=0 mult=1 m=1
XM37 net10 D4 net24 GND sky130_fd_pr__nfet_01v8 L={len_p} W={wid_p} nf=1 ad='int((nf+1)/2) * W/nf * 0.29'
+ as='int((nf+2)/2) * W/nf * 0.29' pd='2*int((nf+1)/2) * (W/nf + 0.29)' ps='2*int((nf+2)/2) * (W/nf + 0.29)'
+ nrd='0.29 / W' nrs='0.29 / W' sa=0 sb=0 sd=0 mult=1 m=1
XM38 net14 D4 net10 GND sky130_fd_pr__nfet_01v8 L={len_p} W={wid_p} nf=1 ad='int((nf+1)/2) * W/nf * 0.29'
+ as='int((nf+2)/2) * W/nf * 0.29' pd='2*int((nf+1)/2) * (W/nf + 0.29)' ps='2*int((nf+2)/2) * (W/nf + 0.29)'
+ nrd='0.29 / W' nrs='0.29 / W' sa=0 sb=0 sd=0 mult=1 m=1
XM39 net8 D5 net11 GND sky130_fd_pr__nfet_01v8 L={len_p} W={wid_p} nf=1 ad='int((nf+1)/2) * W/nf * 0.29'
+ as='int((nf+2)/2) * W/nf * 0.29' pd='2*int((nf+1)/2) * (W/nf + 0.29)' ps='2*int((nf+2)/2) * (W/nf + 0.29)'
+ nrd='0.29 / W' nrs='0.29 / W' sa=0 sb=0 sd=0 mult=1 m=1
XM40 net11 D5 net23 GND sky130_fd_pr__nfet_01v8 L={len_p} W={wid_p} nf=1 ad='int((nf+1)/2) * W/nf * 0.29'
+ as='int((nf+2)/2) * W/nf * 0.29' pd='2*int((nf+1)/2) * (W/nf + 0.29)' ps='2*int((nf+2)/2) * (W/nf + 0.29)'
+ nrd='0.29 / W' nrs='0.29 / W' sa=0 sb=0 sd=0 mult=1 m=1
XM41 net12 D6 net22 GND sky130_fd_pr__nfet_01v8 L={len_p} W={wid_p} nf=1 ad='int((nf+1)/2) * W/nf * 0.29'
+ as='int((nf+2)/2) * W/nf * 0.29' pd='2*int((nf+1)/2) * (W/nf + 0.29)' ps='2*int((nf+2)/2) * (W/nf + 0.29)'
+ nrd='0.29 / W' nrs='0.29 / W' sa=0 sb=0 sd=0 mult=1 m=1
XM42 net6 D6 net12 GND sky130_fd_pr__nfet_01v8 L={len_p} W={wid_p} nf=1 ad='int((nf+1)/2) * W/nf * 0.29'
+ as='int((nf+2)/2) * W/nf * 0.29' pd='2*int((nf+1)/2) * (W/nf + 0.29)' ps='2*int((nf+2)/2) * (W/nf + 0.29)'
+ nrd='0.29 / W' nrs='0.29 / W' sa=0 sb=0 sd=0 mult=1 m=1
XM25 net27 Vbn net16 GND sky130_fd_pr__nfet_01v8 L={len_b} W={wid_b} nf=1 ad='int((nf+1)/2) * W/nf * 0.29'
+ as='int((nf+2)/2) * W/nf * 0.29' pd='2*int((nf+1)/2) * (W/nf + 0.29)' ps='2*int((nf+2)/2) * (W/nf + 0.29)'
+ nrd='0.29 / W' nrs='0.29 / W' sa=0 sb=0 sd=0 mult=1 m=1
XM26 net26 Vbn net17 GND sky130_fd_pr__nfet_01v8 L={len_b} W={wid_b} nf=1 ad='int((nf+1)/2) * W/nf * 0.29'
+ as='int((nf+2)/2) * W/nf * 0.29' pd='2*int((nf+1)/2) * (W/nf + 0.29)' ps='2*int((nf+2)/2) * (W/nf + 0.29)'
+ nrd='0.29 / W' nrs='0.29 / W' sa=0 sb=0 sd=0 mult=1 m=1
XM27 net25 Vbn net18 GND sky130_fd_pr__nfet_01v8 L={len_b} W={wid_b} nf=1 ad='int((nf+1)/2) * W/nf * 0.29'
+ as='int((nf+2)/2) * W/nf * 0.29' pd='2*int((nf+1)/2) * (W/nf + 0.29)' ps='2*int((nf+2)/2) * (W/nf + 0.29)'
+ nrd='0.29 / W' nrs='0.29 / W' sa=0 sb=0 sd=0 mult=1 m=1
XM28 net24 Vbn net19 GND sky130_fd_pr__nfet_01v8 L={len_b} W={wid_b} nf=1 ad='int((nf+1)/2) * W/nf * 0.29'
+ as='int((nf+2)/2) * W/nf * 0.29' pd='2*int((nf+1)/2) * (W/nf + 0.29)' ps='2*int((nf+2)/2) * (W/nf + 0.29)'
+ nrd='0.29 / W' nrs='0.29 / W' sa=0 sb=0 sd=0 mult=1 m=1
XM29 net23 Vbn net20 GND sky130_fd_pr__nfet_01v8 L={len_b} W={wid_b} nf=1 ad='int((nf+1)/2) * W/nf * 0.29'
+ as='int((nf+2)/2) * W/nf * 0.29' pd='2*int((nf+1)/2) * (W/nf + 0.29)' ps='2*int((nf+2)/2) * (W/nf + 0.29)'
+ nrd='0.29 / W' nrs='0.29 / W' sa=0 sb=0 sd=0 mult=1 m=1
XM30 net22 Vbn net21 GND sky130_fd_pr__nfet_01v8 L={len_b} W={wid_b} nf=1 ad='int((nf+1)/2) * W/nf * 0.29'
+ as='int((nf+2)/2) * W/nf * 0.29' pd='2*int((nf+1)/2) * (W/nf + 0.29)' ps='2*int((nf+2)/2) * (W/nf + 0.29)'
+ nrd='0.29 / W' nrs='0.29 / W' sa=0 sb=0 sd=0 mult=1 m=1
.ends

.GLOBAL VDD
.GLOBAL GND
.end
